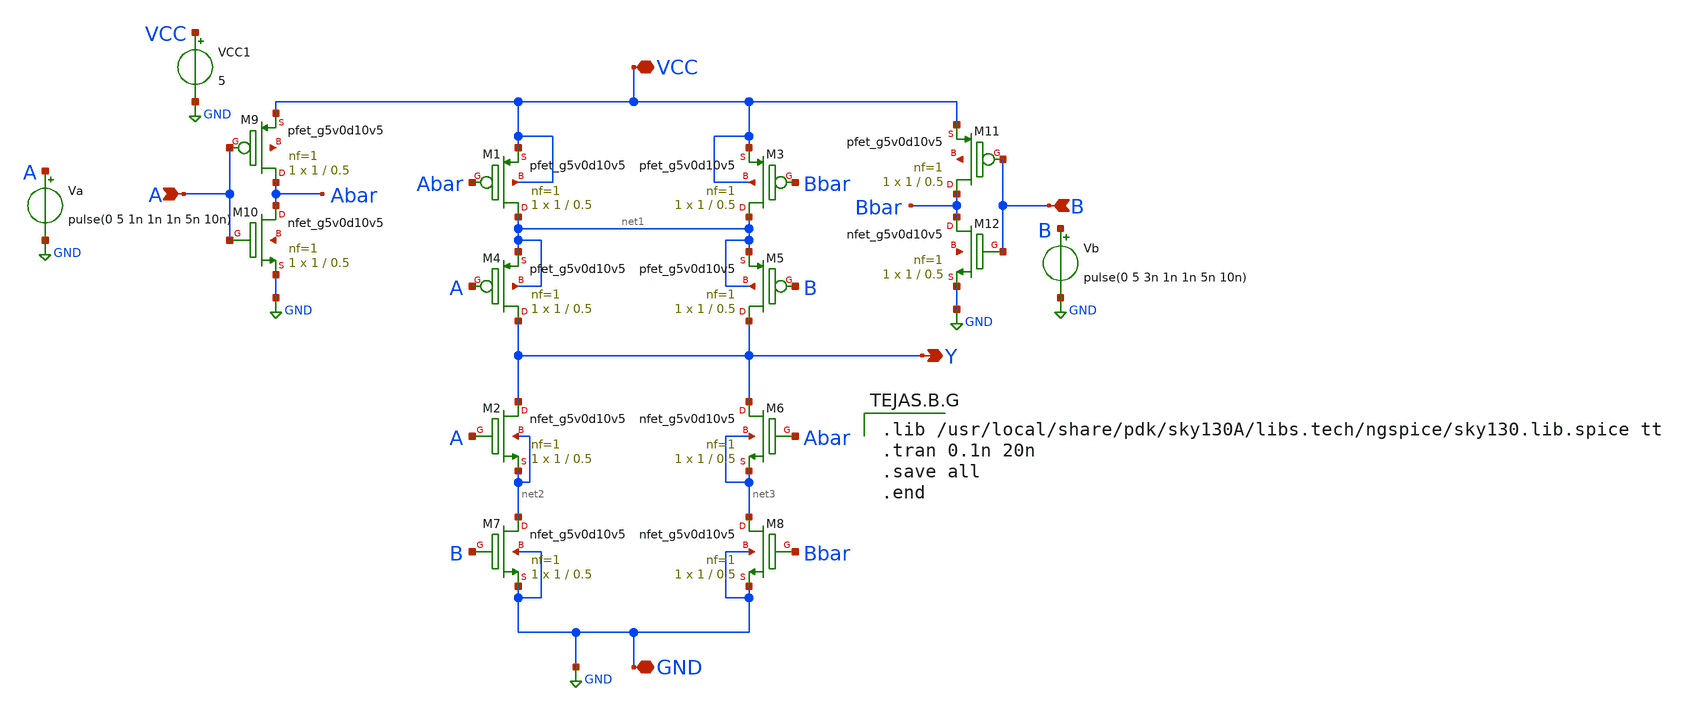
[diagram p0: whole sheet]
** sch_path: Schematic Simulation/Final Simulation/2ipXOR.sch
**.subckt 2ipXOR Y A VCC GND B
*.opin Y
*.ipin A
*.iopin VCC
*.iopin GND
*.ipin B
XM1 net1 Abar VCC VCC sky130_fd_pr__pfet_g5v0d10v5 L=0.5 W=1 nf=1 ad='int((nf+1)/2) * W/nf * 0.29' as='int((nf+2)/2) * W/nf * 0.29'
+ pd='2*int((nf+1)/2) * (W/nf + 0.29)' ps='2*int((nf+2)/2) * (W/nf + 0.29)' nrd='0.29 / W' nrs='0.29 / W'
+ sa=0 sb=0 sd=0 mult=1 m=1
XM2 Y A net2 net2 sky130_fd_pr__nfet_g5v0d10v5 L=0.5 W=1 nf=1 ad='int((nf+1)/2) * W/nf * 0.29' as='int((nf+2)/2) * W/nf * 0.29'
+ pd='2*int((nf+1)/2) * (W/nf + 0.29)' ps='2*int((nf+2)/2) * (W/nf + 0.29)' nrd='0.29 / W' nrs='0.29 / W'
+ sa=0 sb=0 sd=0 mult=1 m=1
XM3 net1 Bbar VCC VCC sky130_fd_pr__pfet_g5v0d10v5 L=0.5 W=1 nf=1 ad='int((nf+1)/2) * W/nf * 0.29' as='int((nf+2)/2) * W/nf * 0.29'
+ pd='2*int((nf+1)/2) * (W/nf + 0.29)' ps='2*int((nf+2)/2) * (W/nf + 0.29)' nrd='0.29 / W' nrs='0.29 / W'
+ sa=0 sb=0 sd=0 mult=1 m=1
XM4 Y A net1 net1 sky130_fd_pr__pfet_g5v0d10v5 L=0.5 W=1 nf=1 ad='int((nf+1)/2) * W/nf * 0.29' as='int((nf+2)/2) * W/nf * 0.29'
+ pd='2*int((nf+1)/2) * (W/nf + 0.29)' ps='2*int((nf+2)/2) * (W/nf + 0.29)' nrd='0.29 / W' nrs='0.29 / W'
+ sa=0 sb=0 sd=0 mult=1 m=1
XM5 Y B net1 net1 sky130_fd_pr__pfet_g5v0d10v5 L=0.5 W=1 nf=1 ad='int((nf+1)/2) * W/nf * 0.29' as='int((nf+2)/2) * W/nf * 0.29'
+ pd='2*int((nf+1)/2) * (W/nf + 0.29)' ps='2*int((nf+2)/2) * (W/nf + 0.29)' nrd='0.29 / W' nrs='0.29 / W'
+ sa=0 sb=0 sd=0 mult=1 m=1
XM6 Y Abar net3 net3 sky130_fd_pr__nfet_g5v0d10v5 L=0.5 W=1 nf=1 ad='int((nf+1)/2) * W/nf * 0.29' as='int((nf+2)/2) * W/nf * 0.29'
+ pd='2*int((nf+1)/2) * (W/nf + 0.29)' ps='2*int((nf+2)/2) * (W/nf + 0.29)' nrd='0.29 / W' nrs='0.29 / W'
+ sa=0 sb=0 sd=0 mult=1 m=1
XM7 net2 B GND GND sky130_fd_pr__nfet_g5v0d10v5 L=0.5 W=1 nf=1 ad='int((nf+1)/2) * W/nf * 0.29' as='int((nf+2)/2) * W/nf * 0.29'
+ pd='2*int((nf+1)/2) * (W/nf + 0.29)' ps='2*int((nf+2)/2) * (W/nf + 0.29)' nrd='0.29 / W' nrs='0.29 / W'
+ sa=0 sb=0 sd=0 mult=1 m=1
XM8 net3 Bbar GND GND sky130_fd_pr__nfet_g5v0d10v5 L=0.5 W=1 nf=1 ad='int((nf+1)/2) * W/nf * 0.29' as='int((nf+2)/2) * W/nf * 0.29'
+ pd='2*int((nf+1)/2) * (W/nf + 0.29)' ps='2*int((nf+2)/2) * (W/nf + 0.29)' nrd='0.29 / W' nrs='0.29 / W'
+ sa=0 sb=0 sd=0 mult=1 m=1
XM9 Abar A VCC net4 sky130_fd_pr__pfet_g5v0d10v5 L=0.5 W=1 nf=1 ad='int((nf+1)/2) * W/nf * 0.29' as='int((nf+2)/2) * W/nf * 0.29'
+ pd='2*int((nf+1)/2) * (W/nf + 0.29)' ps='2*int((nf+2)/2) * (W/nf + 0.29)' nrd='0.29 / W' nrs='0.29 / W'
+ sa=0 sb=0 sd=0 mult=1 m=1
XM10 Abar A GND net5 sky130_fd_pr__nfet_g5v0d10v5 L=0.5 W=1 nf=1 ad='int((nf+1)/2) * W/nf * 0.29' as='int((nf+2)/2) * W/nf * 0.29'
+ pd='2*int((nf+1)/2) * (W/nf + 0.29)' ps='2*int((nf+2)/2) * (W/nf + 0.29)' nrd='0.29 / W' nrs='0.29 / W'
+ sa=0 sb=0 sd=0 mult=1 m=1
XM11 Bbar B VCC net6 sky130_fd_pr__pfet_g5v0d10v5 L=0.5 W=1 nf=1 ad='int((nf+1)/2) * W/nf * 0.29' as='int((nf+2)/2) * W/nf * 0.29'
+ pd='2*int((nf+1)/2) * (W/nf + 0.29)' ps='2*int((nf+2)/2) * (W/nf + 0.29)' nrd='0.29 / W' nrs='0.29 / W'
+ sa=0 sb=0 sd=0 mult=1 m=1
XM12 Bbar B GND net7 sky130_fd_pr__nfet_g5v0d10v5 L=0.5 W=1 nf=1 ad='int((nf+1)/2) * W/nf * 0.29' as='int((nf+2)/2) * W/nf * 0.29'
+ pd='2*int((nf+1)/2) * (W/nf + 0.29)' ps='2*int((nf+2)/2) * (W/nf + 0.29)' nrd='0.29 / W' nrs='0.29 / W'
+ sa=0 sb=0 sd=0 mult=1 m=1
VCC1 VCC GND 5
Va A GND pulse(0 5 1n 1n 1n 5n 10n)
Vb B GND pulse(0 5 3n 1n 1n 5n 10n)
**** begin user architecture code

.lib /usr/local/share/pdk/sky130A/libs.tech/ngspice/sky130.lib.spice tt
.tran 0.1n 20n
.save all
.end

**** end user architecture code
**.ends
.GLOBAL GND
.end
